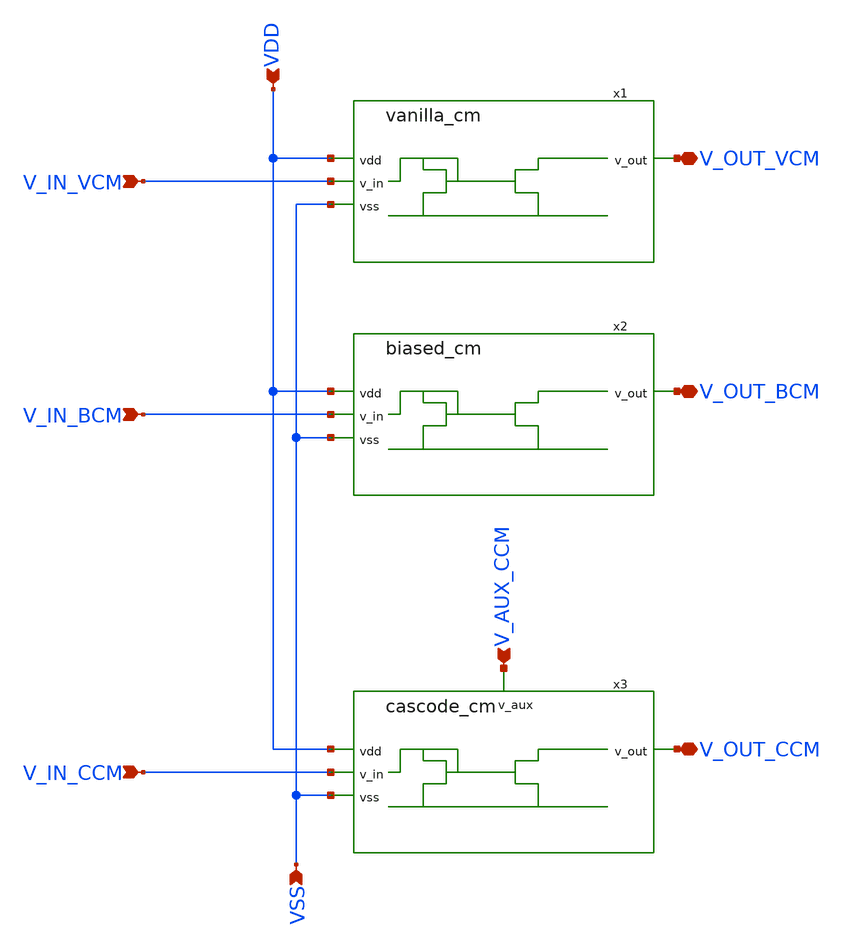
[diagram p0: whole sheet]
** sch_path: blocks/composite/regulated_cascoded_cmirror/xschem/top_level.sch
**.subckt top_level VSS V_IN_BCM V_AUX_CCM VDD V_OUT_VCM V_OUT_BCM V_OUT_CCM V_IN_CCM V_IN_VCM
*.ipin VSS
*.ipin V_IN_BCM
*.ipin V_AUX_CCM
*.ipin VDD
*.iopin V_OUT_VCM
*.iopin V_OUT_BCM
*.iopin V_OUT_CCM
*.ipin V_IN_CCM
*.ipin V_IN_VCM
x1 VDD V_IN_VCM V_OUT_VCM VSS vanilla_cm
x2 VDD V_IN_BCM V_OUT_BCM VSS biased_cm
x3 VDD V_IN_CCM V_OUT_CCM VSS V_AUX_CCM cascode_cm
**.ends

* expanding   symbol:  vanilla_cm.sym # of pins=4
** sym_path: blocks/composite/regulated_cascoded_cmirror/xschem/vanilla_cm.sym
** sch_path: blocks/composite/regulated_cascoded_cmirror/xschem/vanilla_cm.sch
.subckt vanilla_cm vdd v_in v_out vss
*.ipin v_in
*.ipin vdd
*.ipin vss
*.iopin v_out
XM1 v_out net1 vss vss nfet_03v3 L=1u W=5u nf=1 ad='int((nf+1)/2) * W/nf * 0.18u' as='int((nf+2)/2) * W/nf * 0.18u'
+ pd='2*int((nf+1)/2) * (W/nf + 0.18u)' ps='2*int((nf+2)/2) * (W/nf + 0.18u)' nrd='0.18u / W' nrs='0.18u / W'
+ sa=0 sb=0 sd=0 m=1
XM2 net1 net1 vss vss nfet_03v3 L=1u W=5u nf=1 ad='int((nf+1)/2) * W/nf * 0.18u' as='int((nf+2)/2) * W/nf * 0.18u'
+ pd='2*int((nf+1)/2) * (W/nf + 0.18u)' ps='2*int((nf+2)/2) * (W/nf + 0.18u)' nrd='0.18u / W' nrs='0.18u / W'
+ sa=0 sb=0 sd=0 m=1
XM9 net1 v_in vdd vdd pfet_03v3 L=1u W=5u nf=1 ad='int((nf+1)/2) * W/nf * 0.18u' as='int((nf+2)/2) * W/nf * 0.18u'
+ pd='2*int((nf+1)/2) * (W/nf + 0.18u)' ps='2*int((nf+2)/2) * (W/nf + 0.18u)' nrd='0.18u / W' nrs='0.18u / W'
+ sa=0 sb=0 sd=0 m=1
.ends


* expanding   symbol:  biased_cm.sym # of pins=4
** sym_path: blocks/composite/regulated_cascoded_cmirror/xschem/biased_cm.sym
** sch_path: blocks/composite/regulated_cascoded_cmirror/xschem/biased_cm.sch
.subckt biased_cm vdd v_in v_out vss
*.ipin v_in
*.ipin vdd
*.ipin vss
*.iopin v_out
XM3 net2 net1 vss vss nfet_03v3 L=1u W=5u nf=1 ad='int((nf+1)/2) * W/nf * 0.18u' as='int((nf+2)/2) * W/nf * 0.18u'
+ pd='2*int((nf+1)/2) * (W/nf + 0.18u)' ps='2*int((nf+2)/2) * (W/nf + 0.18u)' nrd='0.18u / W' nrs='0.18u / W'
+ sa=0 sb=0 sd=0 m=1
XM4 net1 net1 vss vss nfet_03v3 L=1u W=5u nf=1 ad='int((nf+1)/2) * W/nf * 0.18u' as='int((nf+2)/2) * W/nf * 0.18u'
+ pd='2*int((nf+1)/2) * (W/nf + 0.18u)' ps='2*int((nf+2)/2) * (W/nf + 0.18u)' nrd='0.18u / W' nrs='0.18u / W'
+ sa=0 sb=0 sd=0 m=1
XM5 v_out net3 net2 vss nfet_03v3 L=1u W=5u nf=1 ad='int((nf+1)/2) * W/nf * 0.18u' as='int((nf+2)/2) * W/nf * 0.18u'
+ pd='2*int((nf+1)/2) * (W/nf + 0.18u)' ps='2*int((nf+2)/2) * (W/nf + 0.18u)' nrd='0.18u / W' nrs='0.18u / W'
+ sa=0 sb=0 sd=0 m=1
XM6 net3 net3 net1 vss nfet_03v3 L=1u W=5u nf=1 ad='int((nf+1)/2) * W/nf * 0.18u' as='int((nf+2)/2) * W/nf * 0.18u'
+ pd='2*int((nf+1)/2) * (W/nf + 0.18u)' ps='2*int((nf+2)/2) * (W/nf + 0.18u)' nrd='0.18u / W' nrs='0.18u / W'
+ sa=0 sb=0 sd=0 m=1
XM15 net3 v_in vdd vdd pfet_03v3 L=1u W=5u nf=1 ad='int((nf+1)/2) * W/nf * 0.18u' as='int((nf+2)/2) * W/nf * 0.18u'
+ pd='2*int((nf+1)/2) * (W/nf + 0.18u)' ps='2*int((nf+2)/2) * (W/nf + 0.18u)' nrd='0.18u / W' nrs='0.18u / W'
+ sa=0 sb=0 sd=0 m=1
.ends


* expanding   symbol:  cascode_cm.sym # of pins=5
** sym_path: blocks/composite/regulated_cascoded_cmirror/xschem/cascode_cm.sym
** sch_path: blocks/composite/regulated_cascoded_cmirror/xschem/cascode_cm.sch
.subckt cascode_cm vdd v_in v_out vss v_aux
*.ipin v_in
*.ipin vdd
*.ipin vss
*.ipin v_aux
*.iopin v_out
XM10 net2 net1 vss vss nfet_03v3 L=1u W=5u nf=1 ad='int((nf+1)/2) * W/nf * 0.18u' as='int((nf+2)/2) * W/nf * 0.18u'
+ pd='2*int((nf+1)/2) * (W/nf + 0.18u)' ps='2*int((nf+2)/2) * (W/nf + 0.18u)' nrd='0.18u / W' nrs='0.18u / W'
+ sa=0 sb=0 sd=0 m=1
XM8 net4 net2 net1 vss nfet_03v3 L=1u W=5u nf=1 ad='int((nf+1)/2) * W/nf * 0.18u' as='int((nf+2)/2) * W/nf * 0.18u'
+ pd='2*int((nf+1)/2) * (W/nf + 0.18u)' ps='2*int((nf+2)/2) * (W/nf + 0.18u)' nrd='0.18u / W' nrs='0.18u / W'
+ sa=0 sb=0 sd=0 m=1
XM11 net1 net4 vss vss nfet_03v3 L=1u W=5u nf=1 ad='int((nf+1)/2) * W/nf * 0.18u' as='int((nf+2)/2) * W/nf * 0.18u'
+ pd='2*int((nf+1)/2) * (W/nf + 0.18u)' ps='2*int((nf+2)/2) * (W/nf + 0.18u)' nrd='0.18u / W' nrs='0.18u / W'
+ sa=0 sb=0 sd=0 m=1
XM12 net2 net3 vss vss nfet_03v3 L=1u W=5u nf=1 ad='int((nf+1)/2) * W/nf * 0.18u' as='int((nf+2)/2) * W/nf * 0.18u'
+ pd='2*int((nf+1)/2) * (W/nf + 0.18u)' ps='2*int((nf+2)/2) * (W/nf + 0.18u)' nrd='0.18u / W' nrs='0.18u / W'
+ sa=0 sb=0 sd=0 m=1
XM13 net3 net4 vss vss nfet_03v3 L=1u W=5u nf=1 ad='int((nf+1)/2) * W/nf * 0.18u' as='int((nf+2)/2) * W/nf * 0.18u'
+ pd='2*int((nf+1)/2) * (W/nf + 0.18u)' ps='2*int((nf+2)/2) * (W/nf + 0.18u)' nrd='0.18u / W' nrs='0.18u / W'
+ sa=0 sb=0 sd=0 m=1
XM14 v_out net2 net3 vss nfet_03v3 L=1u W=5u nf=1 ad='int((nf+1)/2) * W/nf * 0.18u' as='int((nf+2)/2) * W/nf * 0.18u'
+ pd='2*int((nf+1)/2) * (W/nf + 0.18u)' ps='2*int((nf+2)/2) * (W/nf + 0.18u)' nrd='0.18u / W' nrs='0.18u / W'
+ sa=0 sb=0 sd=0 m=1
XM16 net4 v_in vdd vdd pfet_03v3 L=1u W=5u nf=1 ad='int((nf+1)/2) * W/nf * 0.18u' as='int((nf+2)/2) * W/nf * 0.18u'
+ pd='2*int((nf+1)/2) * (W/nf + 0.18u)' ps='2*int((nf+2)/2) * (W/nf + 0.18u)' nrd='0.18u / W' nrs='0.18u / W'
+ sa=0 sb=0 sd=0 m=1
XM18 net2 v_aux vdd vdd pfet_03v3 L=1u W=5u nf=1 ad='int((nf+1)/2) * W/nf * 0.18u' as='int((nf+2)/2) * W/nf * 0.18u'
+ pd='2*int((nf+1)/2) * (W/nf + 0.18u)' ps='2*int((nf+2)/2) * (W/nf + 0.18u)' nrd='0.18u / W' nrs='0.18u / W'
+ sa=0 sb=0 sd=0 m=1
.ends

.end
